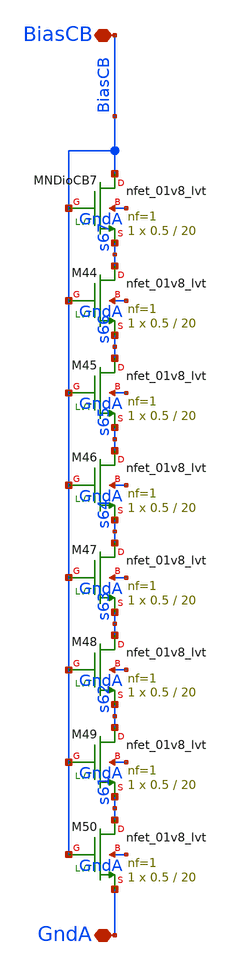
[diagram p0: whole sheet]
** sch_path: analog/klayout/production/final_merge_20260923/testbenches/cace/analog/xschem/BiasCoarseMB_DIV_W005_L200_8.sch
**.subckt BiasCoarseMB_DIV_W005_L200_8 BiasCB GndA
*.iopin BiasCB
*.iopin GndA
XMNDioCB7 BiasCB BiasCB s67 GndA sky130_fd_pr__nfet_01v8_lvt L=20 W=0.5 nf=1 ad='int((1 + 1)/2) * 0.5 / 1 * 0.29'
+ as='int((1 + 2)/2) * 0.5 / 1 * 0.29' pd='2*int((1 + 1)/2) * (0.5 / 1 + 0.29)' ps='2*int((1 + 2)/2) * (0.5 / 1 + 0.29)'
+ nrd='0.29 / 0.5 ' nrs='0.29 / 0.5 ' sa=0 sb=0 sd=0 mult=1 m=1
XM44 s67 BiasCB s66 GndA sky130_fd_pr__nfet_01v8_lvt L=20 W=0.5 nf=1 ad='int((1 + 1)/2) * 0.5 / 1 * 0.29'
+ as='int((1 + 2)/2) * 0.5 / 1 * 0.29' pd='2*int((1 + 1)/2) * (0.5 / 1 + 0.29)' ps='2*int((1 + 2)/2) * (0.5 / 1 + 0.29)'
+ nrd='0.29 / 0.5 ' nrs='0.29 / 0.5 ' sa=0 sb=0 sd=0 mult=1 m=1
XM45 s66 BiasCB s65 GndA sky130_fd_pr__nfet_01v8_lvt L=20 W=0.5 nf=1 ad='int((1 + 1)/2) * 0.5 / 1 * 0.29'
+ as='int((1 + 2)/2) * 0.5 / 1 * 0.29' pd='2*int((1 + 1)/2) * (0.5 / 1 + 0.29)' ps='2*int((1 + 2)/2) * (0.5 / 1 + 0.29)'
+ nrd='0.29 / 0.5 ' nrs='0.29 / 0.5 ' sa=0 sb=0 sd=0 mult=1 m=1
XM46 s65 BiasCB s64 GndA sky130_fd_pr__nfet_01v8_lvt L=20 W=0.5 nf=1 ad='int((1 + 1)/2) * 0.5 / 1 * 0.29'
+ as='int((1 + 2)/2) * 0.5 / 1 * 0.29' pd='2*int((1 + 1)/2) * (0.5 / 1 + 0.29)' ps='2*int((1 + 2)/2) * (0.5 / 1 + 0.29)'
+ nrd='0.29 / 0.5 ' nrs='0.29 / 0.5 ' sa=0 sb=0 sd=0 mult=1 m=1
XM47 s64 BiasCB s63 GndA sky130_fd_pr__nfet_01v8_lvt L=20 W=0.5 nf=1 ad='int((1 + 1)/2) * 0.5 / 1 * 0.29'
+ as='int((1 + 2)/2) * 0.5 / 1 * 0.29' pd='2*int((1 + 1)/2) * (0.5 / 1 + 0.29)' ps='2*int((1 + 2)/2) * (0.5 / 1 + 0.29)'
+ nrd='0.29 / 0.5 ' nrs='0.29 / 0.5 ' sa=0 sb=0 sd=0 mult=1 m=1
XM48 s63 BiasCB s62 GndA sky130_fd_pr__nfet_01v8_lvt L=20 W=0.5 nf=1 ad='int((1 + 1)/2) * 0.5 / 1 * 0.29'
+ as='int((1 + 2)/2) * 0.5 / 1 * 0.29' pd='2*int((1 + 1)/2) * (0.5 / 1 + 0.29)' ps='2*int((1 + 2)/2) * (0.5 / 1 + 0.29)'
+ nrd='0.29 / 0.5 ' nrs='0.29 / 0.5 ' sa=0 sb=0 sd=0 mult=1 m=1
XM49 s62 BiasCB s61 GndA sky130_fd_pr__nfet_01v8_lvt L=20 W=0.5 nf=1 ad='int((1 + 1)/2) * 0.5 / 1 * 0.29'
+ as='int((1 + 2)/2) * 0.5 / 1 * 0.29' pd='2*int((1 + 1)/2) * (0.5 / 1 + 0.29)' ps='2*int((1 + 2)/2) * (0.5 / 1 + 0.29)'
+ nrd='0.29 / 0.5 ' nrs='0.29 / 0.5 ' sa=0 sb=0 sd=0 mult=1 m=1
XM50 s61 BiasCB GndA GndA sky130_fd_pr__nfet_01v8_lvt L=20 W=0.5 nf=1 ad='int((1 + 1)/2) * 0.5 / 1 * 0.29'
+ as='int((1 + 2)/2) * 0.5 / 1 * 0.29' pd='2*int((1 + 1)/2) * (0.5 / 1 + 0.29)' ps='2*int((1 + 2)/2) * (0.5 / 1 + 0.29)'
+ nrd='0.29 / 0.5 ' nrs='0.29 / 0.5 ' sa=0 sb=0 sd=0 mult=1 m=1
**.ends
.end
